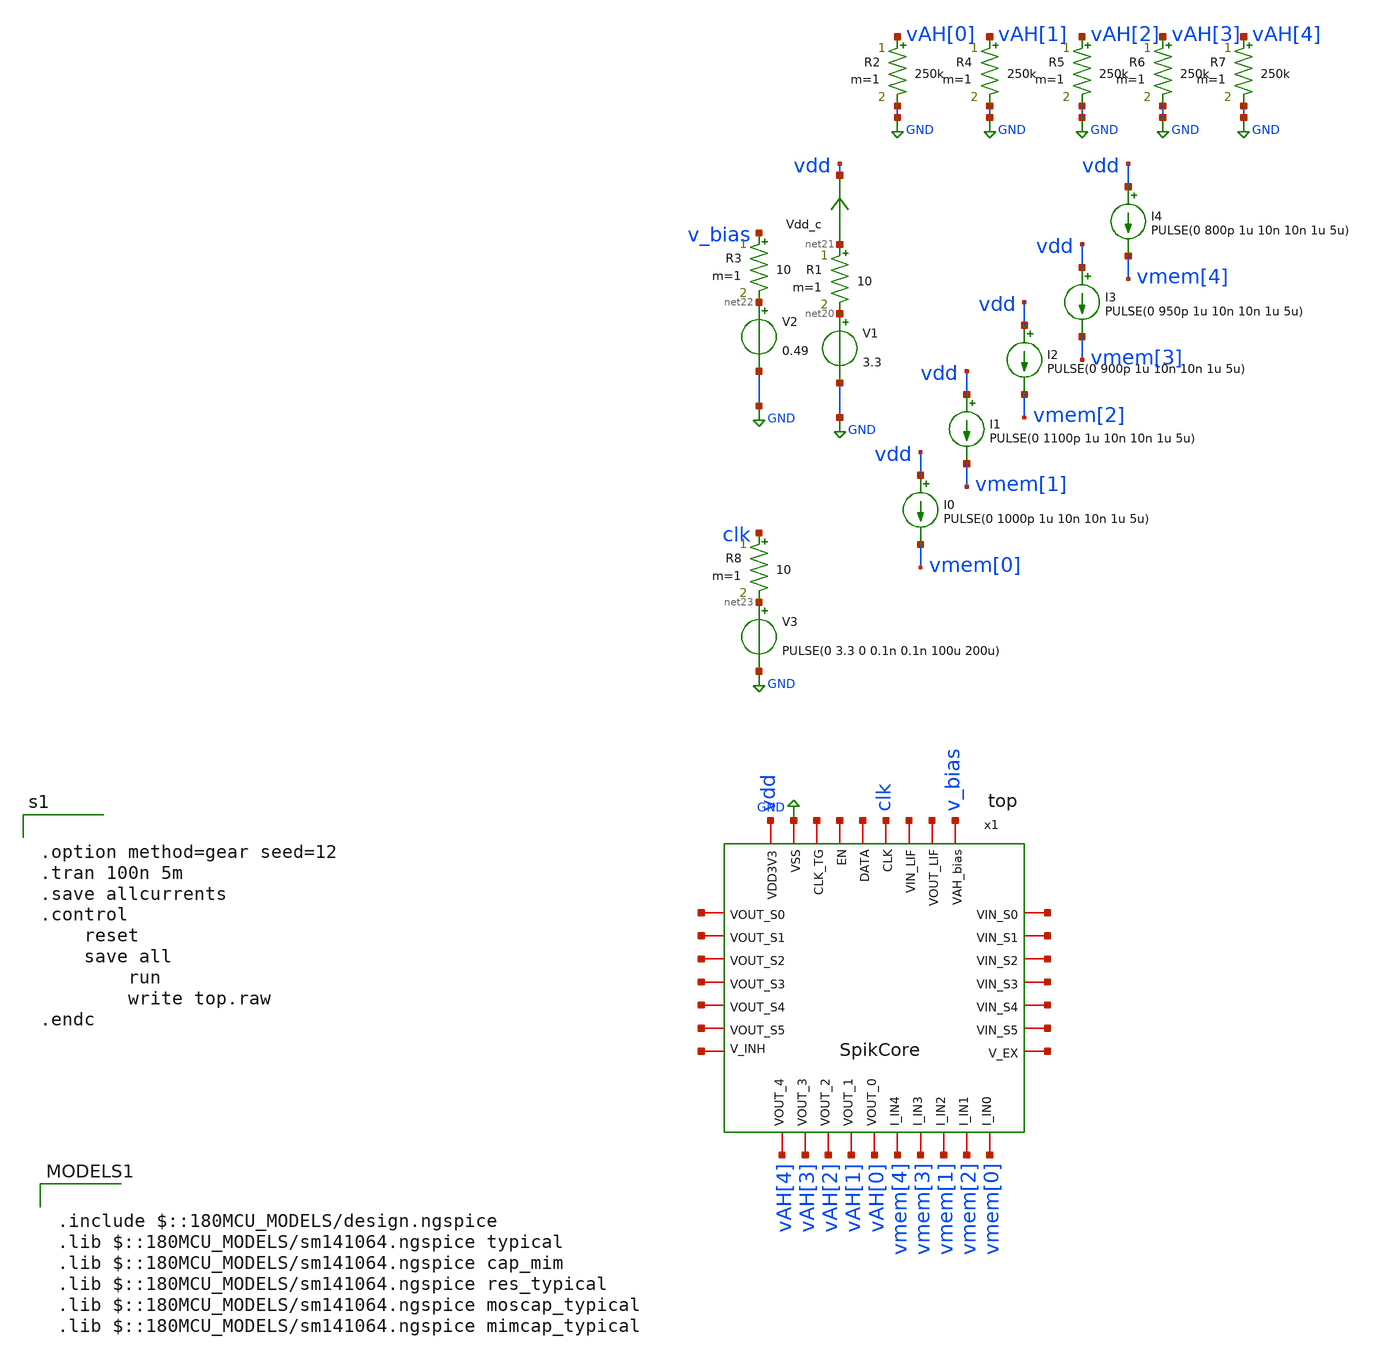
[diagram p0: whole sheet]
** sch_path: designs/libs/tb_top/top.sch
**.subckt top
x1 vdd GND net1 net2 net3 clk net4 net5 net6 net7 net8 net9 net10 net11 net12 net13 net14 net15
+ net16 net17 net18 net19 vmem[0] vAH[0] vmem[2] vAH[1] vmem[1] vAH[2] vmem[3] vAH[3] vmem[4] vAH[4] v_bias
+ top
V1 net20 GND 3.3
Vdd_c net21 vdd 0
.save i(vdd_c)
I0 vdd vmem[0] PULSE(0 1000p 1u 10n 10n 1u 5u)
R1 net21 net20 10 m=1
R2 vAH[0] GND 250k m=1
V2 net22 GND 0.49
R3 v_bias net22 10 m=1
R4 vAH[1] GND 250k m=1
R5 vAH[2] GND 250k m=1
R6 vAH[3] GND 250k m=1
I1 vdd vmem[1] PULSE(0 1100p 1u 10n 10n 1u 5u)
I2 vdd vmem[2] PULSE(0 900p 1u 10n 10n 1u 5u)
I3 vdd vmem[3] PULSE(0 950p 1u 10n 10n 1u 5u)
R7 vAH[4] GND 250k m=1
I4 vdd vmem[4] PULSE(0 800p 1u 10n 10n 1u 5u)
V3 net23 GND PULSE(0 3.3 0 0.1n 0.1n 100u 200u)
R8 clk net23 10 m=1
**** begin user architecture code

.include $::180MCU_MODELS/design.ngspice
.lib $::180MCU_MODELS/sm141064.ngspice typical
.lib $::180MCU_MODELS/sm141064.ngspice cap_mim
.lib $::180MCU_MODELS/sm141064.ngspice res_typical
.lib $::180MCU_MODELS/sm141064.ngspice moscap_typical
.lib $::180MCU_MODELS/sm141064.ngspice mimcap_typical



.option method=gear seed=12
.tran 100n 5m
.save allcurrents
.control
	reset
	save all
        run
        write top.raw
.endc


**** end user architecture code
**.ends
.GLOBAL GND
.end
